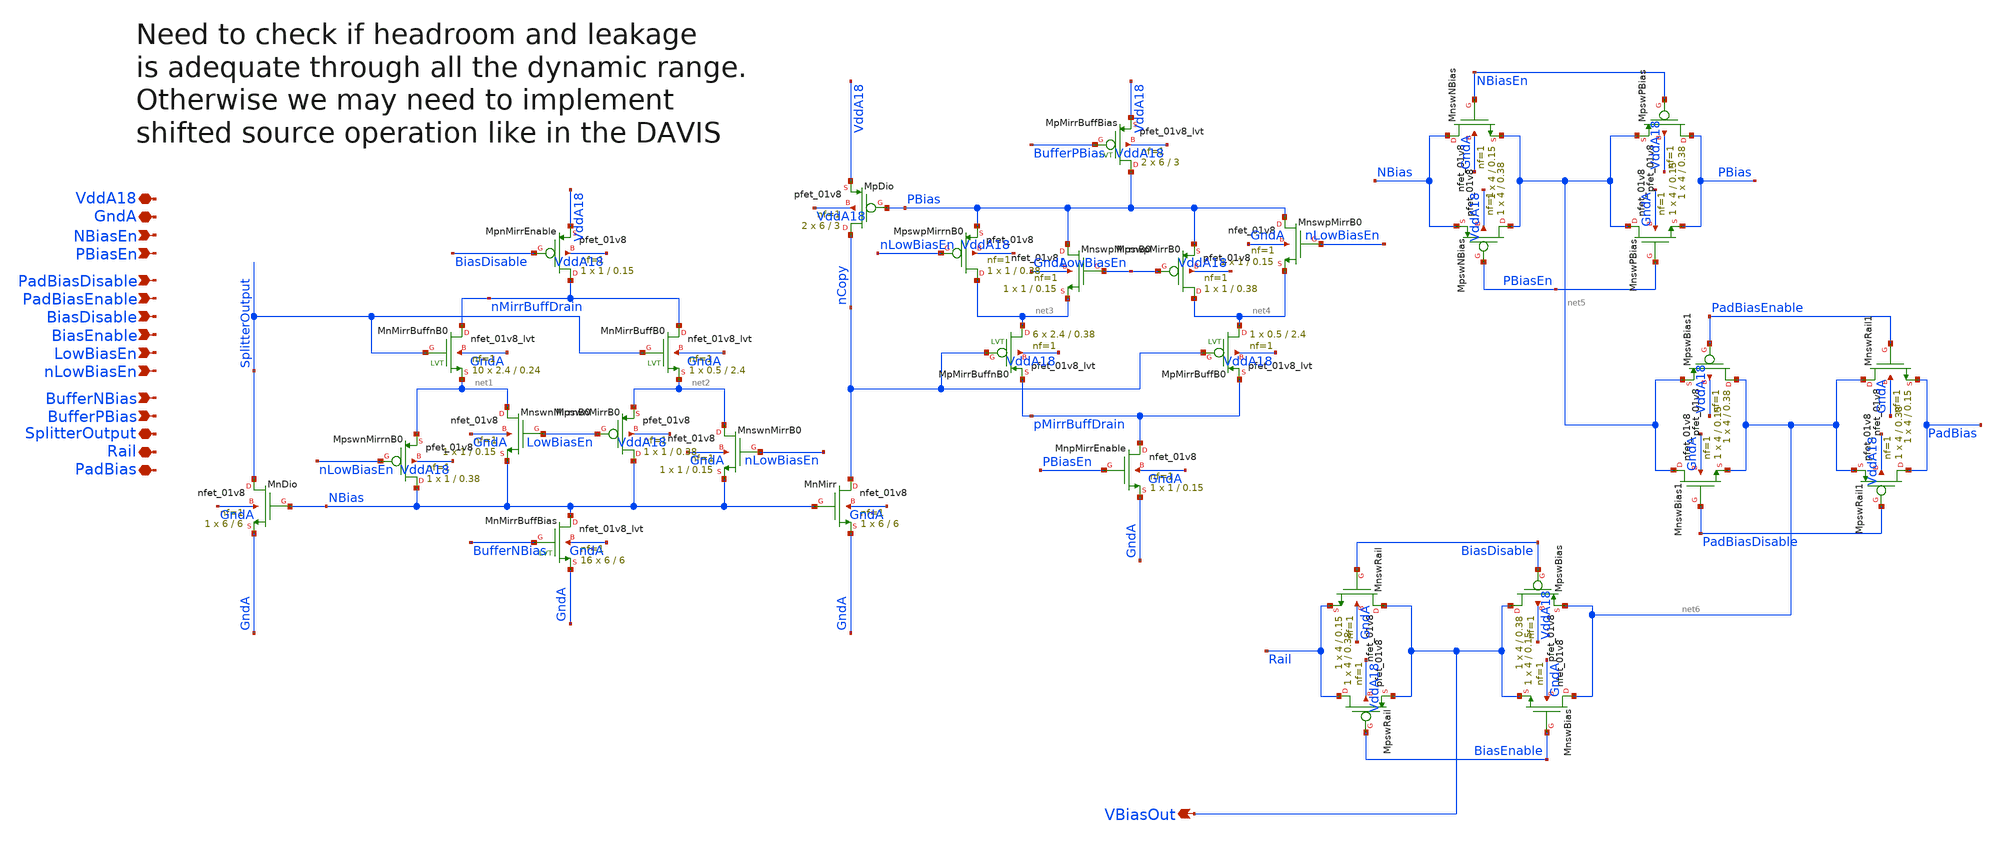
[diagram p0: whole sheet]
** sch_path: analog/xschem/BiasBuffers.sch
**.subckt BiasBuffers GndA VddA18 VBiasOut NBiasEn PBiasEn BiasDisable BiasEnable LowBiasEn
*+ BufferNBias BufferPBias SplitterOutput Rail nLowBiasEn PadBiasDisable PadBiasEnable PadBias
*.iopin GndA
*.iopin VddA18
*.opin VBiasOut
*.ipin NBiasEn
*.ipin PBiasEn
*.ipin BiasDisable
*.ipin BiasEnable
*.ipin LowBiasEn
*.ipin BufferNBias
*.ipin BufferPBias
*.iopin SplitterOutput
*.iopin Rail
*.ipin nLowBiasEn
*.ipin PadBiasDisable
*.ipin PadBiasEnable
*.iopin PadBias
XMnDio SplitterOutput NBias GndA GndA sky130_fd_pr__nfet_01v8 L=6 W=6 nf=1 ad='int((1 + 1)/2) * 6 / 1 * 0.29'
+ as='int((1 + 2)/2) * 6 / 1 * 0.29' pd='2*int((1 + 1)/2) * (6 / 1 + 0.29)' ps='2*int((1 + 2)/2) * (6 / 1 + 0.29)'
+ nrd='0.29 / 6 ' nrs='0.29 / 6 ' sa=0 sb=0 sd=0 mult=1 m=1
XMnswnMirrnB0 net1 LowBiasEn NBias GndA sky130_fd_pr__nfet_01v8 L=0.15 W=1 nf=1 ad='int((1 + 1)/2) * 1 / 1 * 0.29'
+ as='int((1 + 2)/2) * 1 / 1 * 0.29' pd='2*int((1 + 1)/2) * (1 / 1 + 0.29)' ps='2*int((1 + 2)/2) * (1 / 1 + 0.29)'
+ nrd='0.29 / 1 ' nrs='0.29 / 1 ' sa=0 sb=0 sd=0 mult=1 m=1
XMpswnMirrnB0 NBias nLowBiasEn net1 VddA18 sky130_fd_pr__pfet_01v8 L=0.38 W=1 nf=1 ad='int((1 + 1)/2) * 1 / 1 * 0.29'
+ as='int((1 + 2)/2) * 1 / 1 * 0.29' pd='2*int((1 + 1)/2) * (1 / 1 + 0.29)' ps='2*int((1 + 2)/2) * (1 / 1 + 0.29)'
+ nrd='0.29 / 1 ' nrs='0.29 / 1 ' sa=0 sb=0 sd=0 mult=1 m=1
XMnMirrBuffB0 nMirrBuffDrain SplitterOutput net2 GndA sky130_fd_pr__nfet_01v8_lvt L=2.4 W=0.5 nf=1 ad='int((1 + 1)/2) * 0.5 / 1 * 0.29'
+ as='int((1 + 2)/2) * 0.5 / 1 * 0.29' pd='2*int((1 + 1)/2) * (0.5 / 1 + 0.29)' ps='2*int((1 + 2)/2) * (0.5 / 1 + 0.29)'
+ nrd='0.29 / 0.5 ' nrs='0.29 / 0.5 ' sa=0 sb=0 sd=0 mult=1 m=1
XMpnMirrEnable nMirrBuffDrain BiasDisable VddA18 VddA18 sky130_fd_pr__pfet_01v8 L=0.15 W=1 nf=1 ad='int((1 + 1)/2) * 1 / 1 * 0.29'
+ as='int((1 + 2)/2) * 1 / 1 * 0.29' pd='2*int((1 + 1)/2) * (1 / 1 + 0.29)' ps='2*int((1 + 2)/2) * (1 / 1 + 0.29)'
+ nrd='0.29 / 1 ' nrs='0.29 / 1 ' sa=0 sb=0 sd=0 mult=1 m=1
XMnswnMirrB0 net2 nLowBiasEn NBias GndA sky130_fd_pr__nfet_01v8 L=0.15 W=1 nf=1 ad='int((1 + 1)/2) * 1 / 1 * 0.29'
+ as='int((1 + 2)/2) * 1 / 1 * 0.29' pd='2*int((1 + 1)/2) * (1 / 1 + 0.29)' ps='2*int((1 + 2)/2) * (1 / 1 + 0.29)'
+ nrd='0.29 / 1 ' nrs='0.29 / 1 ' sa=0 sb=0 sd=0 mult=1 m=1
XMpswnMirrB0 NBias LowBiasEn net2 VddA18 sky130_fd_pr__pfet_01v8 L=0.38 W=1 nf=1 ad='int((1 + 1)/2) * 1 / 1 * 0.29'
+ as='int((1 + 2)/2) * 1 / 1 * 0.29' pd='2*int((1 + 1)/2) * (1 / 1 + 0.29)' ps='2*int((1 + 2)/2) * (1 / 1 + 0.29)'
+ nrd='0.29 / 1 ' nrs='0.29 / 1 ' sa=0 sb=0 sd=0 mult=1 m=1
XMnMirr nCopy NBias GndA GndA sky130_fd_pr__nfet_01v8 L=6 W=6 nf=1 ad='int((1 + 1)/2) * 6 / 1 * 0.29'
+ as='int((1 + 2)/2) * 6 / 1 * 0.29' pd='2*int((1 + 1)/2) * (6 / 1 + 0.29)' ps='2*int((1 + 2)/2) * (6 / 1 + 0.29)'
+ nrd='0.29 / 6 ' nrs='0.29 / 6 ' sa=0 sb=0 sd=0 mult=1 m=1
XMnMirrBuffBias NBias BufferNBias GndA GndA sky130_fd_pr__nfet_01v8_lvt L=6 W=6 nf=1 ad='int((1 + 1)/2) * 6 / 1 * 0.29'
+ as='int((1 + 2)/2) * 6 / 1 * 0.29' pd='2*int((1 + 1)/2) * (6 / 1 + 0.29)' ps='2*int((1 + 2)/2) * (6 / 1 + 0.29)'
+ nrd='0.29 / 6 ' nrs='0.29 / 6 ' sa=0 sb=0 sd=0 mult=16 m=16
XMpDio nCopy PBias VddA18 VddA18 sky130_fd_pr__pfet_01v8 L=3 W=6 nf=1 ad='int((1 + 1)/2) * 6 / 1 * 0.29'
+ as='int((1 + 2)/2) * 6 / 1 * 0.29' pd='2*int((1 + 1)/2) * (6 / 1 + 0.29)' ps='2*int((1 + 2)/2) * (6 / 1 + 0.29)'
+ nrd='0.29 / 6 ' nrs='0.29 / 6 ' sa=0 sb=0 sd=0 mult=2 m=2
XMnswpMirrnB0 PBias LowBiasEn net3 GndA sky130_fd_pr__nfet_01v8 L=0.15 W=1 nf=1 ad='int((1 + 1)/2) * 1 / 1 * 0.29'
+ as='int((1 + 2)/2) * 1 / 1 * 0.29' pd='2*int((1 + 1)/2) * (1 / 1 + 0.29)' ps='2*int((1 + 2)/2) * (1 / 1 + 0.29)'
+ nrd='0.29 / 1 ' nrs='0.29 / 1 ' sa=0 sb=0 sd=0 mult=1 m=1
XMpswpMirrnB0 net3 nLowBiasEn PBias VddA18 sky130_fd_pr__pfet_01v8 L=0.38 W=1 nf=1 ad='int((1 + 1)/2) * 1 / 1 * 0.29'
+ as='int((1 + 2)/2) * 1 / 1 * 0.29' pd='2*int((1 + 1)/2) * (1 / 1 + 0.29)' ps='2*int((1 + 2)/2) * (1 / 1 + 0.29)'
+ nrd='0.29 / 1 ' nrs='0.29 / 1 ' sa=0 sb=0 sd=0 mult=1 m=1
XMnswpMirrB0 PBias nLowBiasEn net4 GndA sky130_fd_pr__nfet_01v8 L=0.15 W=1 nf=1 ad='int((1 + 1)/2) * 1 / 1 * 0.29'
+ as='int((1 + 2)/2) * 1 / 1 * 0.29' pd='2*int((1 + 1)/2) * (1 / 1 + 0.29)' ps='2*int((1 + 2)/2) * (1 / 1 + 0.29)'
+ nrd='0.29 / 1 ' nrs='0.29 / 1 ' sa=0 sb=0 sd=0 mult=1 m=1
XMpswpMirrB0 net4 LowBiasEn PBias VddA18 sky130_fd_pr__pfet_01v8 L=0.38 W=1 nf=1 ad='int((1 + 1)/2) * 1 / 1 * 0.29'
+ as='int((1 + 2)/2) * 1 / 1 * 0.29' pd='2*int((1 + 1)/2) * (1 / 1 + 0.29)' ps='2*int((1 + 2)/2) * (1 / 1 + 0.29)'
+ nrd='0.29 / 1 ' nrs='0.29 / 1 ' sa=0 sb=0 sd=0 mult=1 m=1
XMpMirrBuffnB0 net3 nCopy pMirrBuffDrain VddA18 sky130_fd_pr__pfet_01v8_lvt L=0.38 W=2.4 nf=1 ad='int((1 + 1)/2) * 2.4 / 1 * 0.29'
+ as='int((1 + 2)/2) * 2.4 / 1 * 0.29' pd='2*int((1 + 1)/2) * (2.4 / 1 + 0.29)' ps='2*int((1 + 2)/2) * (2.4 / 1 + 0.29)'
+ nrd='0.29 / 2.4 ' nrs='0.29 / 2.4 ' sa=0 sb=0 sd=0 mult=6 m=6
XMpMirrBuffB0 net4 nCopy pMirrBuffDrain VddA18 sky130_fd_pr__pfet_01v8_lvt L=2.4 W=0.5 nf=1 ad='int((1 + 1)/2) * 0.5 / 1 * 0.29'
+ as='int((1 + 2)/2) * 0.5 / 1 * 0.29' pd='2*int((1 + 1)/2) * (0.5 / 1 + 0.29)' ps='2*int((1 + 2)/2) * (0.5 / 1 + 0.29)'
+ nrd='0.29 / 0.5 ' nrs='0.29 / 0.5 ' sa=0 sb=0 sd=0 mult=1 m=1
XMnpMirrEnable pMirrBuffDrain PBiasEn GndA GndA sky130_fd_pr__nfet_01v8 L=0.15 W=1 nf=1 ad='int((1 + 1)/2) * 1 / 1 * 0.29'
+ as='int((1 + 2)/2) * 1 / 1 * 0.29' pd='2*int((1 + 1)/2) * (1 / 1 + 0.29)' ps='2*int((1 + 2)/2) * (1 / 1 + 0.29)'
+ nrd='0.29 / 1 ' nrs='0.29 / 1 ' sa=0 sb=0 sd=0 mult=1 m=1
XMpMirrBuffBias PBias BufferPBias VddA18 VddA18 sky130_fd_pr__pfet_01v8_lvt L=3 W=6 nf=1 ad='int((1 + 1)/2) * 6 / 1 * 0.29'
+ as='int((1 + 2)/2) * 6 / 1 * 0.29' pd='2*int((1 + 1)/2) * (6 / 1 + 0.29)' ps='2*int((1 + 2)/2) * (6 / 1 + 0.29)'
+ nrd='0.29 / 6 ' nrs='0.29 / 6 ' sa=0 sb=0 sd=0 mult=2 m=2
XMnswNBias NBias NBiasEn net5 GndA sky130_fd_pr__nfet_01v8 L=0.15 W=4 nf=1 ad='int((1 + 1)/2) * 4 / 1 * 0.29'
+ as='int((1 + 2)/2) * 4 / 1 * 0.29' pd='2*int((1 + 1)/2) * (4 / 1 + 0.29)' ps='2*int((1 + 2)/2) * (4 / 1 + 0.29)'
+ nrd='0.29 / 4 ' nrs='0.29 / 4 ' sa=0 sb=0 sd=0 mult=1 m=1
XMpswNBias net5 PBiasEn NBias VddA18 sky130_fd_pr__pfet_01v8 L=0.38 W=4 nf=1 ad='int((1 + 1)/2) * 4 / 1 * 0.29'
+ as='int((1 + 2)/2) * 4 / 1 * 0.29' pd='2*int((1 + 1)/2) * (4 / 1 + 0.29)' ps='2*int((1 + 2)/2) * (4 / 1 + 0.29)'
+ nrd='0.29 / 4 ' nrs='0.29 / 4 ' sa=0 sb=0 sd=0 mult=1 m=1
XMnswPBias net5 PBiasEn PBias GndA sky130_fd_pr__nfet_01v8 L=0.15 W=4 nf=1 ad='int((1 + 1)/2) * 4 / 1 * 0.29'
+ as='int((1 + 2)/2) * 4 / 1 * 0.29' pd='2*int((1 + 1)/2) * (4 / 1 + 0.29)' ps='2*int((1 + 2)/2) * (4 / 1 + 0.29)'
+ nrd='0.29 / 4 ' nrs='0.29 / 4 ' sa=0 sb=0 sd=0 mult=1 m=1
XMpswPBias PBias NBiasEn net5 VddA18 sky130_fd_pr__pfet_01v8 L=0.38 W=4 nf=1 ad='int((1 + 1)/2) * 4 / 1 * 0.29'
+ as='int((1 + 2)/2) * 4 / 1 * 0.29' pd='2*int((1 + 1)/2) * (4 / 1 + 0.29)' ps='2*int((1 + 2)/2) * (4 / 1 + 0.29)'
+ nrd='0.29 / 4 ' nrs='0.29 / 4 ' sa=0 sb=0 sd=0 mult=1 m=1
XMnswBias net6 BiasEnable VBiasOut GndA sky130_fd_pr__nfet_01v8 L=0.15 W=4 nf=1 ad='int((1 + 1)/2) * 4 / 1 * 0.29'
+ as='int((1 + 2)/2) * 4 / 1 * 0.29' pd='2*int((1 + 1)/2) * (4 / 1 + 0.29)' ps='2*int((1 + 2)/2) * (4 / 1 + 0.29)'
+ nrd='0.29 / 4 ' nrs='0.29 / 4 ' sa=0 sb=0 sd=0 mult=1 m=1
XMpswBias VBiasOut BiasDisable net6 VddA18 sky130_fd_pr__pfet_01v8 L=0.38 W=4 nf=1 ad='int((1 + 1)/2) * 4 / 1 * 0.29'
+ as='int((1 + 2)/2) * 4 / 1 * 0.29' pd='2*int((1 + 1)/2) * (4 / 1 + 0.29)' ps='2*int((1 + 2)/2) * (4 / 1 + 0.29)'
+ nrd='0.29 / 4 ' nrs='0.29 / 4 ' sa=0 sb=0 sd=0 mult=1 m=1
XMnswRail VBiasOut BiasDisable Rail GndA sky130_fd_pr__nfet_01v8 L=0.15 W=4 nf=1 ad='int((1 + 1)/2) * 4 / 1 * 0.29'
+ as='int((1 + 2)/2) * 4 / 1 * 0.29' pd='2*int((1 + 1)/2) * (4 / 1 + 0.29)' ps='2*int((1 + 2)/2) * (4 / 1 + 0.29)'
+ nrd='0.29 / 4 ' nrs='0.29 / 4 ' sa=0 sb=0 sd=0 mult=1 m=1
XMpswRail Rail BiasEnable VBiasOut VddA18 sky130_fd_pr__pfet_01v8 L=0.38 W=4 nf=1 ad='int((1 + 1)/2) * 4 / 1 * 0.29'
+ as='int((1 + 2)/2) * 4 / 1 * 0.29' pd='2*int((1 + 1)/2) * (4 / 1 + 0.29)' ps='2*int((1 + 2)/2) * (4 / 1 + 0.29)'
+ nrd='0.29 / 4 ' nrs='0.29 / 4 ' sa=0 sb=0 sd=0 mult=1 m=1
XMnMirrBuffnB0 nMirrBuffDrain SplitterOutput net1 GndA sky130_fd_pr__nfet_01v8_lvt L=0.24 W=2.4 nf=1
+ ad='int((1 + 1)/2) * 2.4 / 1 * 0.29' as='int((1 + 2)/2) * 2.4 / 1 * 0.29' pd='2*int((1 + 1)/2) * (2.4 / 1 + 0.29)'
+ ps='2*int((1 + 2)/2) * (2.4 / 1 + 0.29)' nrd='0.29 / 2.4 ' nrs='0.29 / 2.4 ' sa=0 sb=0 sd=0 mult=10 m=10
XMnswBias1 net5 PadBiasDisable net6 GndA sky130_fd_pr__nfet_01v8 L=0.15 W=4 nf=1 ad='int((1 + 1)/2) * 4 / 1 * 0.29'
+ as='int((1 + 2)/2) * 4 / 1 * 0.29' pd='2*int((1 + 1)/2) * (4 / 1 + 0.29)' ps='2*int((1 + 2)/2) * (4 / 1 + 0.29)'
+ nrd='0.29 / 4 ' nrs='0.29 / 4 ' sa=0 sb=0 sd=0 mult=1 m=1
XMpswBias1 net6 PadBiasEnable net5 VddA18 sky130_fd_pr__pfet_01v8 L=0.38 W=4 nf=1 ad='int((1 + 1)/2) * 4 / 1 * 0.29'
+ as='int((1 + 2)/2) * 4 / 1 * 0.29' pd='2*int((1 + 1)/2) * (4 / 1 + 0.29)' ps='2*int((1 + 2)/2) * (4 / 1 + 0.29)'
+ nrd='0.29 / 4 ' nrs='0.29 / 4 ' sa=0 sb=0 sd=0 mult=1 m=1
XMnswRail1 net6 PadBiasEnable PadBias GndA sky130_fd_pr__nfet_01v8 L=0.15 W=4 nf=1 ad='int((1 + 1)/2) * 4 / 1 * 0.29'
+ as='int((1 + 2)/2) * 4 / 1 * 0.29' pd='2*int((1 + 1)/2) * (4 / 1 + 0.29)' ps='2*int((1 + 2)/2) * (4 / 1 + 0.29)'
+ nrd='0.29 / 4 ' nrs='0.29 / 4 ' sa=0 sb=0 sd=0 mult=1 m=1
XMpswRail1 PadBias PadBiasDisable net6 VddA18 sky130_fd_pr__pfet_01v8 L=0.38 W=4 nf=1 ad='int((1 + 1)/2) * 4 / 1 * 0.29'
+ as='int((1 + 2)/2) * 4 / 1 * 0.29' pd='2*int((1 + 1)/2) * (4 / 1 + 0.29)' ps='2*int((1 + 2)/2) * (4 / 1 + 0.29)'
+ nrd='0.29 / 4 ' nrs='0.29 / 4 ' sa=0 sb=0 sd=0 mult=1 m=1
**.ends
.end
